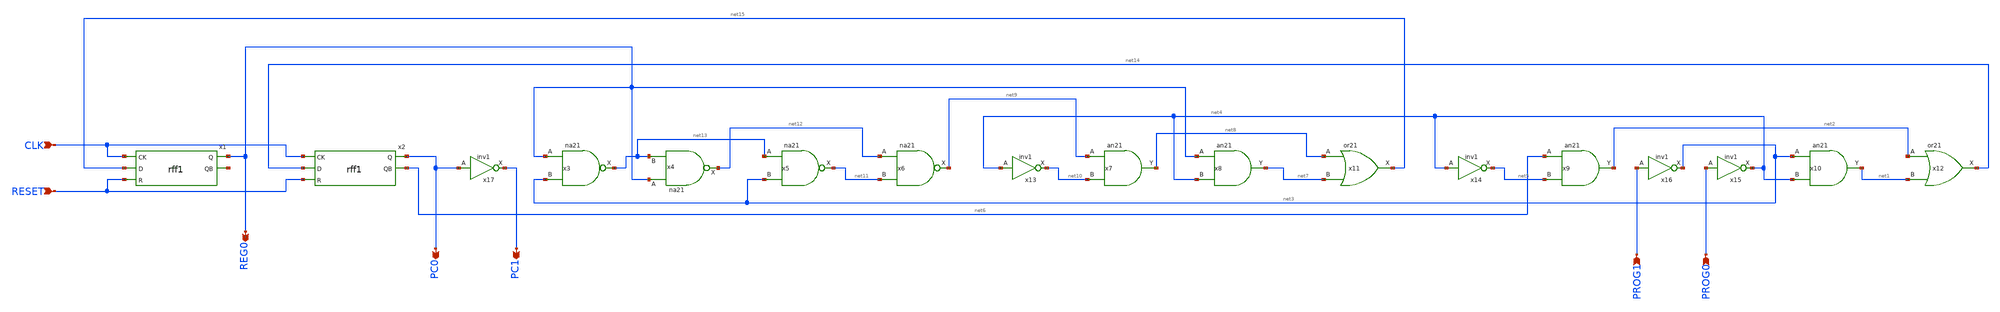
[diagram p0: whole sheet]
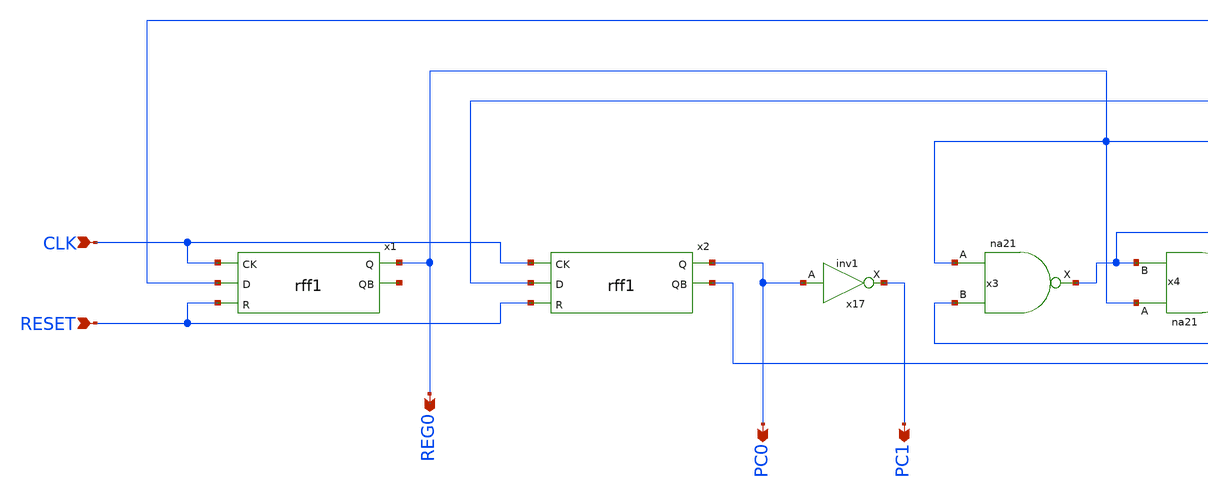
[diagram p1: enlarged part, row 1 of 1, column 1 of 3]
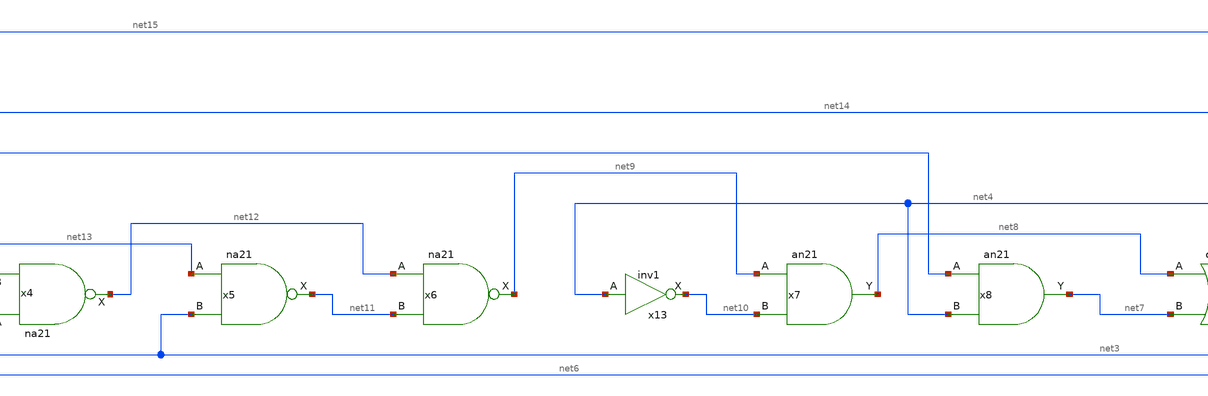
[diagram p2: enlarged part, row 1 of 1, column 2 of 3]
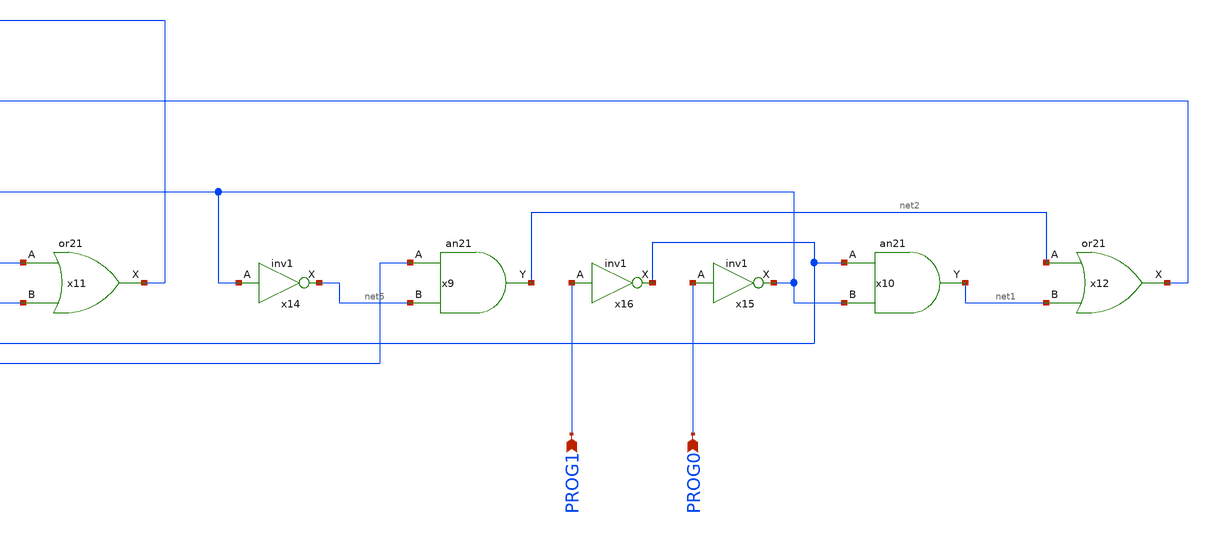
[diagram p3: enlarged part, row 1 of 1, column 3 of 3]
** sch_path: member_project/GxP/xschem/1bit-CPU_1line.sch
**.subckt 1bit-CPU_1line CLK RESET PROG1 PROG0 REG0 PC0 PC1
*.ipin CLK
*.ipin RESET
*.ipin PROG1
*.ipin PROG0
*.opin REG0
*.opin PC0
*.opin PC1
x3 REG0 net3 VDD GND net13 na21
x4 REG0 net13 VDD GND net12 na21
x5 net13 net3 VDD GND net11 na21
x6 net12 net11 VDD GND net9 na21
x7 net9 net10 VDD GND net8 an21
x8 REG0 net4 VDD GND net7 an21
x9 net6 net5 VDD GND net2 an21
x10 net3 net4 VDD GND net1 an21
x13 net4 VDD GND net10 inv1
x14 net4 VDD GND net5 inv1
x15 PROG0 VDD GND net4 inv1
x16 PROG1 VDD GND net3 inv1
x17 PC0 VDD GND PC1 inv1
x11 net8 net7 VDD GND net15 or21
x12 net2 net1 VDD GND net14 or21
x1 CLK net15 REG0 net16 RESET VDD GND rff1
x2 CLK net14 PC0 net6 RESET VDD GND rff1
**.ends
.end
